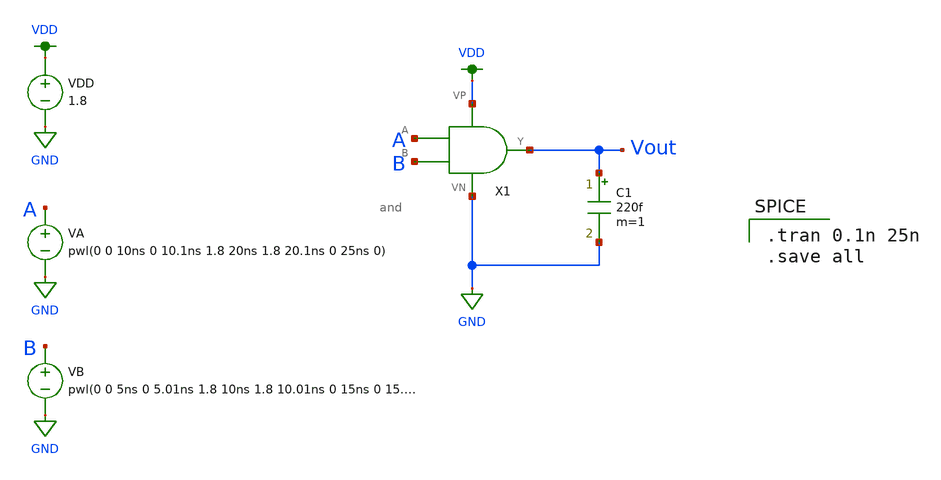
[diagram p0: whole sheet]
** sch_path: MP1/and_tran.sch
**.subckt and_tran
C1 Vout GND 220f m=1
VDD VDD GND 1.8
X1 A B Vout VDD GND and
VA A GND pwl(0 0 10ns 0 10.1ns 1.8 20ns 1.8 20.1ns 0 25ns 0)
VB B GND pwl(0 0 5ns 0 5.01ns 1.8 10ns 1.8 10.01ns 0 15ns 0 15.1ns 1.8 20ns 1.8 20.01ns 0 25ns 0)
**** begin user architecture code

.option wnflag=1
.lib ~/skywater/skywater-pdk/libraries/sky130_fd_pr_ngspice/latest/models/sky130.lib.spice tt


.tran 0.1n 25n
.save all

**** end user architecture code
**.ends
.GLOBAL VDD
.GLOBAL GND
.end
